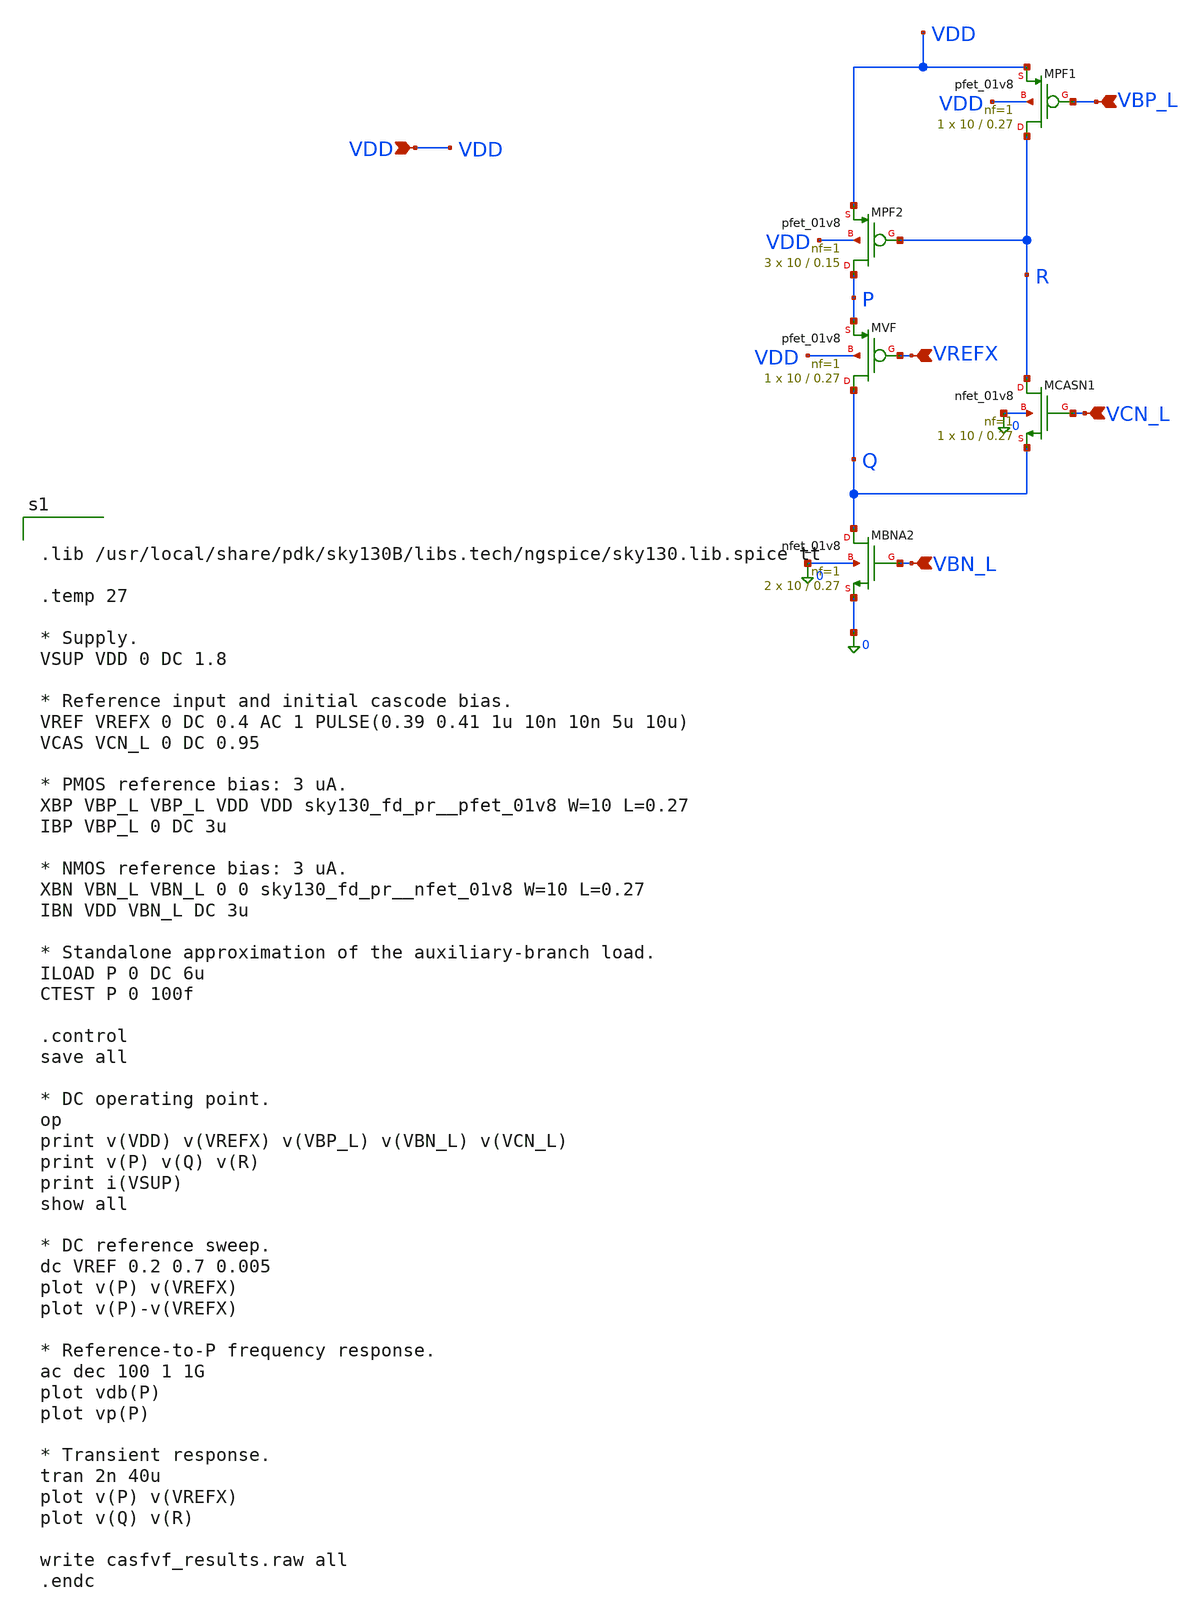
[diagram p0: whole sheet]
** sch_path: CASFVF-1.sch
**.subckt CASFVF-1 VDD VBP_L VREFX VCN_L VBN_L
*.ipin VDD
*.ipin VBP_L
*.ipin VREFX
*.ipin VCN_L
*.ipin VBN_L
XMBNA2 Q VBN_L 0 0 sky130_fd_pr__nfet_01v8 L=0.27 W=10 nf=1 ad='int((1 + 1)/2) * 10 / 1 * 0.29' as='int((1 + 2)/2) * 10 / 1 * 0.29'
+ pd='2*int((1 + 1)/2) * (10 / 1 + 0.29)' ps='2*int((1 + 2)/2) * (10 / 1 + 0.29)' nrd='0.29 / 10 ' nrs='0.29 / 10 '
+ sa=0 sb=0 sd=0 mult=2 m=2
XMPF1 R VBP_L VDD VDD sky130_fd_pr__pfet_01v8 L=0.27 W=10 nf=1 ad='int((1 + 1)/2) * 10 / 1 * 0.29' as='int((1 + 2)/2) * 10 / 1 * 0.29'
+ pd='2*int((1 + 1)/2) * (10 / 1 + 0.29)' ps='2*int((1 + 2)/2) * (10 / 1 + 0.29)' nrd='0.29 / 10 ' nrs='0.29 / 10 '
+ sa=0 sb=0 sd=0 mult=1 m=1
XMCASN1 R VCN_L Q 0 sky130_fd_pr__nfet_01v8 L=0.27 W=10 nf=1 ad='int((1 + 1)/2) * 10 / 1 * 0.29' as='int((1 + 2)/2) * 10 / 1 * 0.29'
+ pd='2*int((1 + 1)/2) * (10 / 1 + 0.29)' ps='2*int((1 + 2)/2) * (10 / 1 + 0.29)' nrd='0.29 / 10 ' nrs='0.29 / 10 '
+ sa=0 sb=0 sd=0 mult=1 m=1
XMPF2 P R VDD VDD sky130_fd_pr__pfet_01v8 L=0.15 W=10 nf=1 ad='int((1 + 1)/2) * 10 / 1 * 0.29' as='int((1 + 2)/2) * 10 / 1 * 0.29'
+ pd='2*int((1 + 1)/2) * (10 / 1 + 0.29)' ps='2*int((1 + 2)/2) * (10 / 1 + 0.29)' nrd='0.29 / 10 ' nrs='0.29 / 10 '
+ sa=0 sb=0 sd=0 mult=3 m=3
XMVF Q VREFX P VDD sky130_fd_pr__pfet_01v8 L=0.27 W=10 nf=1 ad='int((1 + 1)/2) * 10 / 1 * 0.29' as='int((1 + 2)/2) * 10 / 1 * 0.29'
+ pd='2*int((1 + 1)/2) * (10 / 1 + 0.29)' ps='2*int((1 + 2)/2) * (10 / 1 + 0.29)' nrd='0.29 / 10 ' nrs='0.29 / 10 '
+ sa=0 sb=0 sd=0 mult=1 m=1
**** begin user architecture code


.lib /usr/local/share/pdk/sky130B/libs.tech/ngspice/sky130.lib.spice tt

.temp 27

* Supply.
VSUP VDD 0 DC 1.8

* Reference input and initial cascode bias.
VREF VREFX 0 DC 0.4 AC 1 PULSE(0.39 0.41 1u 10n 10n 5u 10u)
VCAS VCN_L 0 DC 0.95

* PMOS reference bias: 3 uA.
XBP VBP_L VBP_L VDD VDD sky130_fd_pr__pfet_01v8 W=10 L=0.27
IBP VBP_L 0 DC 3u

* NMOS reference bias: 3 uA.
XBN VBN_L VBN_L 0 0 sky130_fd_pr__nfet_01v8 W=10 L=0.27
IBN VDD VBN_L DC 3u

* Standalone approximation of the auxiliary-branch load.
ILOAD P 0 DC 6u
CTEST P 0 100f

.control
save all

* DC operating point.
op
print v(VDD) v(VREFX) v(VBP_L) v(VBN_L) v(VCN_L)
print v(P) v(Q) v(R)
print i(VSUP)
show all

* DC reference sweep.
dc VREF 0.2 0.7 0.005
plot v(P) v(VREFX)
plot v(P)-v(VREFX)

* Reference-to-P frequency response.
ac dec 100 1 1G
plot vdb(P)
plot vp(P)

* Transient response.
tran 2n 40u
plot v(P) v(VREFX)
plot v(Q) v(R)

write casfvf_results.raw all
.endc


**** end user architecture code
**.ends
.end
